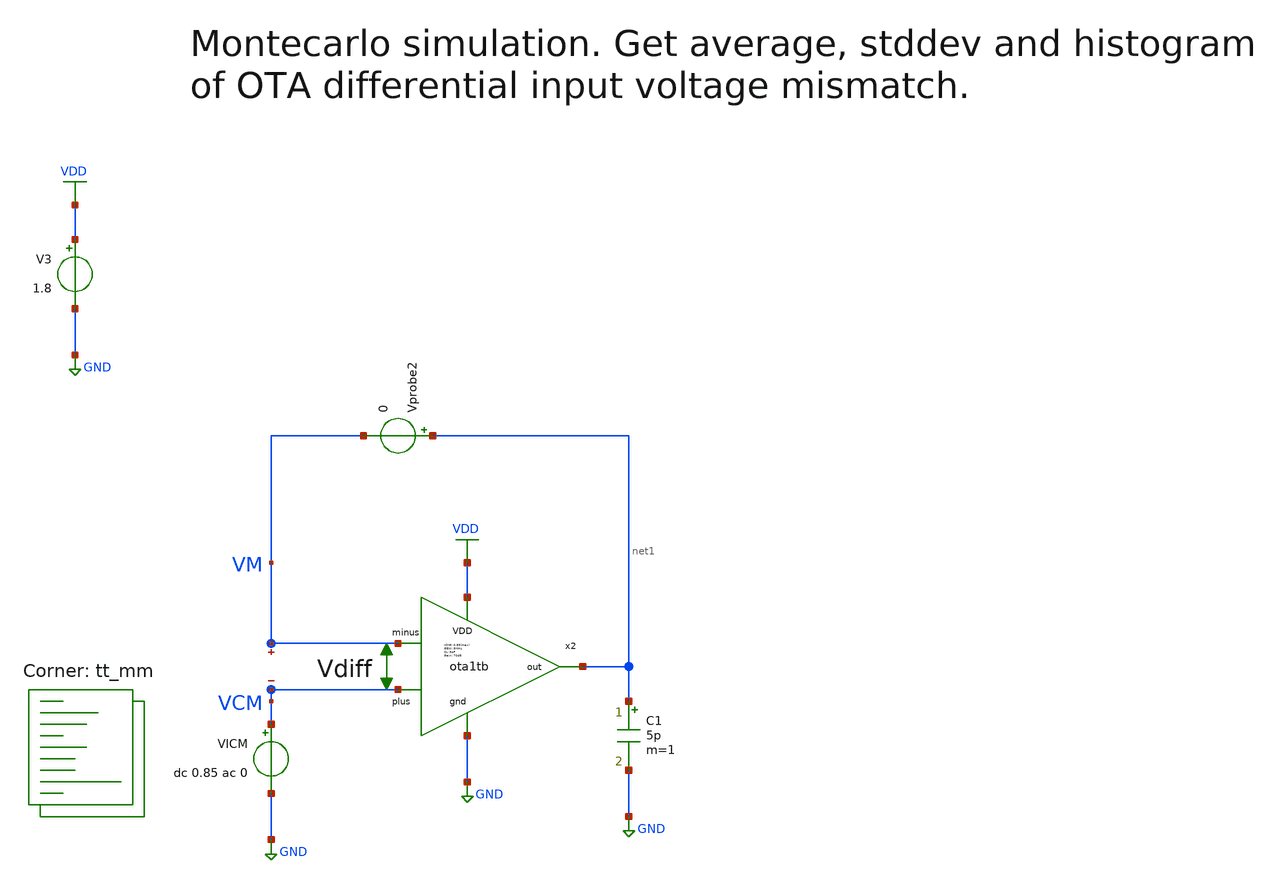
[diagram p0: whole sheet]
** sch_path: sky130A/xschem_libs/sky130_tests/montecarlo_mismatch_sim/schematic/montecarlo_mismatch_sim.sch
**.subckt montecarlo_mismatch_sim
Vprobe2 net1 VM 0
VICM VCM GND dc 0.85 ac 0
C1 net1 GND 5p m=1
V3 VDD GND 1.8
x2 VDD VM VCM net1 GND ota1tb
.save v(vm)
.save v(vcm)
**** begin user architecture code


.options savecurrents
.control
 let runs=1000
 let r=0
 dowhile r < runs
   reset
   op
   let vdiff = v(vm,vcm)
   let run=r
   remzerovec
   write montecarlo_mismatch_sim.raw
   set appendwrite
   print v(vm,vcm)
   let r = r + 1
 end
.endc


.lib $::SKYWATER_MODELS/sky130.lib.spice tt_mm
**** end user architecture code
**.ends

* expanding   symbol:  sky130_tests/ota1tb.sym # of pins=5
** sym_path: sky130_tests/ota1tb.sym
** sch_path: sky130_tests/ota1tb.sch
.subckt ota1tb VDD minus plus out gnd
*.ipin minus
*.ipin plus
*.ipin VDD
*.ipin gnd
*.opin out
XM6 net3 net3 gnd GND sky130_fd_pr__nfet_01v8 L=1.5 W=0.564 nf=1 ad='int((nf+1)/2) * W/nf * 0.29' as='int((nf+2)/2) * W/nf * 0.29'
+ pd='2*int((nf+1)/2) * (W/nf + 0.29)' ps='2*int((nf+2)/2) * (W/nf + 0.29)' nrd='0.29 / W' nrs='0.29 / W'
+ sa=0 sb=0 sd=0 mult=1 m=1
XM8 out Vdiff gnd GND sky130_fd_pr__nfet_01v8 L=0.5 W=12 nf=1 ad='int((nf+1)/2) * W/nf * 0.29' as='int((nf+2)/2) * W/nf * 0.29'
+ pd='2*int((nf+1)/2) * (W/nf + 0.29)' ps='2*int((nf+2)/2) * (W/nf + 0.29)' nrd='0.29 / W' nrs='0.29 / W'
+ sa=0 sb=0 sd=0 mult=1 m=1
XM1 net3 minus net1 VDD sky130_fd_pr__pfet_01v8_lvt L=1.5 W=2.644 nf=2 ad='int((nf+1)/2) * W/nf * 0.29'
+ as='int((nf+2)/2) * W/nf * 0.29' pd='2*int((nf+1)/2) * (W/nf + 0.29)' ps='2*int((nf+2)/2) * (W/nf + 0.29)'
+ nrd='0.29 / W' nrs='0.29 / W' sa=0 sb=0 sd=0 mult=5 m=5
XM3 Vdiff net3 gnd GND sky130_fd_pr__nfet_01v8 L=1.5 W=0.564 nf=1 ad='int((nf+1)/2) * W/nf * 0.29' as='int((nf+2)/2) * W/nf * 0.29'
+ pd='2*int((nf+1)/2) * (W/nf + 0.29)' ps='2*int((nf+2)/2) * (W/nf + 0.29)' nrd='0.29 / W' nrs='0.29 / W'
+ sa=0 sb=0 sd=0 mult=1 m=1
XM4 net1 net2 VDD VDD sky130_fd_pr__pfet_01v8 L=0.75 W=0.515 nf=1 ad='int((nf+1)/2) * W/nf * 0.29' as='int((nf+2)/2) * W/nf * 0.29'
+ pd='2*int((nf+1)/2) * (W/nf + 0.29)' ps='2*int((nf+2)/2) * (W/nf + 0.29)' nrd='0.29 / W' nrs='0.29 / W'
+ sa=0 sb=0 sd=0 mult=4 m=4
XM2 Vdiff plus net1 VDD sky130_fd_pr__pfet_01v8_lvt L=1.5 W=2.644 nf=2 ad='int((nf+1)/2) * W/nf * 0.29'
+ as='int((nf+2)/2) * W/nf * 0.29' pd='2*int((nf+1)/2) * (W/nf + 0.29)' ps='2*int((nf+2)/2) * (W/nf + 0.29)'
+ nrd='0.29 / W' nrs='0.29 / W' sa=0 sb=0 sd=0 mult=5 m=5
XR4 net4 Vdiff gnd sky130_fd_pr__res_xhigh_po_1p41 L=14.5 mult=1 m=1
XC3 out net4 sky130_fd_pr__cap_mim_m3_1 W=1 L=25 MF=20 m=20
XM7 net2 net2 VDD VDD sky130_fd_pr__pfet_01v8 L=0.75 W=0.515 nf=1 ad='int((nf+1)/2) * W/nf * 0.29' as='int((nf+2)/2) * W/nf * 0.29'
+ pd='2*int((nf+1)/2) * (W/nf + 0.29)' ps='2*int((nf+2)/2) * (W/nf + 0.29)' nrd='0.29 / W' nrs='0.29 / W'
+ sa=0 sb=0 sd=0 mult=4 m=4
XM5 out net2 VDD VDD sky130_fd_pr__pfet_01v8 L=0.75 W=0.515 nf=1 ad='int((nf+1)/2) * W/nf * 0.29' as='int((nf+2)/2) * W/nf * 0.29'
+ pd='2*int((nf+1)/2) * (W/nf + 0.29)' ps='2*int((nf+2)/2) * (W/nf + 0.29)' nrd='0.29 / W' nrs='0.29 / W'
+ sa=0 sb=0 sd=0 mult=4 m=4
XR8 net7 net2 gnd sky130_fd_pr__res_xhigh_po_1p41 L=11.75 mult=1 m=1
XR5 net6 net7 gnd sky130_fd_pr__res_xhigh_po_1p41 L=11.75 mult=1 m=1
XR6 net5 net6 gnd sky130_fd_pr__res_xhigh_po_1p41 L=11.75 mult=1 m=1
XR9 gnd net5 gnd sky130_fd_pr__res_xhigh_po_1p41 L=11.75 mult=1 m=1
.ends

.GLOBAL VDD
.GLOBAL GND
.end
